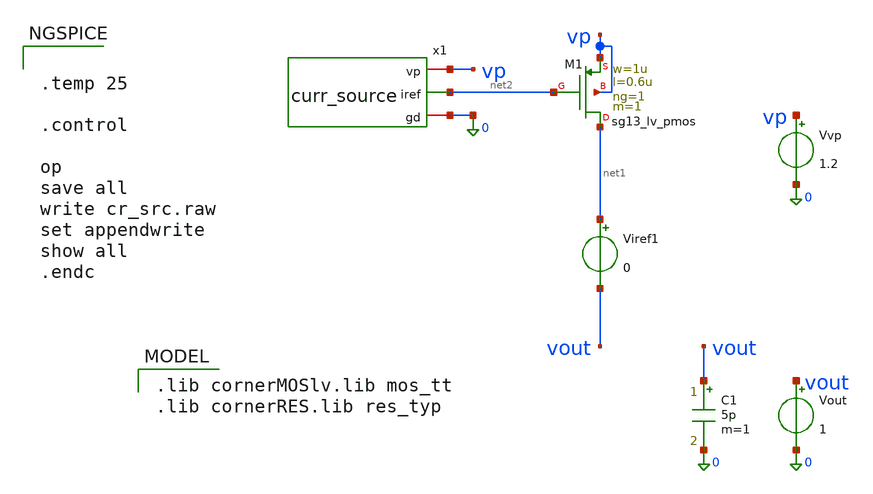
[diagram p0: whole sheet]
** sch_path: PLL0663-main/testbenches/tran/xschem/charge_pump/curr_source_tb.sch
**.subckt curr_source_tb
Vvp vp 0 1.2
Viref1 net1 vout 0
XM1 net1 net2 vp vp sg13_lv_pmos w=1u l=0.6u ng=1 m=1 mm_ok=1
C1 vout 0 5p m=1
Vout vout 0 1
x1 vp net2 0 curr_source
**** begin user architecture code


.temp 25

.control

op
save all
write cr_src.raw
set appendwrite
show all
.endc


 .lib cornerMOSlv.lib mos_tt
.lib cornerRES.lib res_typ




**** end user architecture code
**.ends

* expanding   symbol:
*+  /foss/designs/IHP__PLL0663/PLL0663-main/schematic/xschem/charge_pump/curr_source.sym # of pins=3
** sym_path: /foss/designs/IHP__PLL0663/PLL0663-main/schematic/xschem/charge_pump/curr_source.sym
** sch_path: /foss/designs/IHP__PLL0663/PLL0663-main/schematic/xschem/charge_pump/curr_source.sch
.subckt curr_source vp iref gd
*.iopin vp
*.iopin gd
*.opin iref
XM9 net3 net3 gd gd sg13_lv_nmos w=1u l=0.6u ng=1 m=1 mm_ok=1
XM4 iref iref vp vp sg13_lv_pmos w=1.4u l=0.6u ng=1 m=1 mm_ok=1
XM5 net2 iref vp vp sg13_lv_pmos w=1.2u l=0.6u ng=1 m=1 mm_ok=1
XM10 iref net2 net1 gd sg13_lv_nmos w=1.2u l=0.6u ng=1 m=1 mm_ok=1
XM1 net2 net2 gd gd sg13_lv_nmos w=1.4u l=0.6u ng=1 m=1 mm_ok=1
XM3 vp vp net3 gd sg13_lv_nmos w=1u l=0.6u ng=1 m=1 mm_ok=1
XM6 vp net3 iref gd sg13_lv_nmos w=1u l=0.6u ng=1 m=1 mm_ok=1
XM2 gd gd gd gd sg13_lv_nmos w=0.4u l=0.6u ng=1 m=1 mm_ok=1
XR2 net1 gd gd rppd w=1e-6 l=1.7e-6 m=1 b=0 mm_ok=1
.ends

.end
